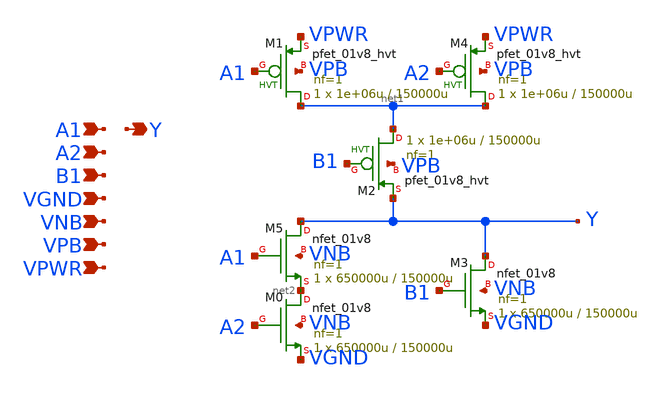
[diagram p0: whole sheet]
** sch_path: schematics/a21oi/sky130_fd_sc_hd__a21oi_1.sch
**.subckt sky130_fd_sc_hd__a21oi_1 A1 A2 B1 VGND VNB VPB VPWR Y
*.ipin A1
*.ipin A2
*.ipin B1
*.ipin VGND
*.ipin VNB
*.ipin VPB
*.ipin VPWR
*.opin Y
XM1 net1 A1 VPWR VPB sky130_fd_pr__pfet_01v8_hvt L=150000u W=1e+06u nf=1 ad='int((1 + 1)/2) * 1e+06u / 1 * 0.29'
+ as='int((1 + 2)/2) * 1e+06u / 1 * 0.29' pd='2*int((1 + 1)/2) * (1e+06u / 1 + 0.29)' ps='2*int((1 + 2)/2) * (1e+06u / 1 + 0.29)'
+ nrd='0.29 / 1e+06u ' nrs='0.29 / 1e+06u ' sa=0 sb=0 sd=0 mult=1 m=1
XM4 net1 A2 VPWR VPB sky130_fd_pr__pfet_01v8_hvt L=150000u W=1e+06u nf=1 ad='int((1 + 1)/2) * 1e+06u / 1 * 0.29'
+ as='int((1 + 2)/2) * 1e+06u / 1 * 0.29' pd='2*int((1 + 1)/2) * (1e+06u / 1 + 0.29)' ps='2*int((1 + 2)/2) * (1e+06u / 1 + 0.29)'
+ nrd='0.29 / 1e+06u ' nrs='0.29 / 1e+06u ' sa=0 sb=0 sd=0 mult=1 m=1
XM2 net1 B1 Y VPB sky130_fd_pr__pfet_01v8_hvt L=150000u W=1e+06u nf=1 ad='int((1 + 1)/2) * 1e+06u / 1 * 0.29'
+ as='int((1 + 2)/2) * 1e+06u / 1 * 0.29' pd='2*int((1 + 1)/2) * (1e+06u / 1 + 0.29)' ps='2*int((1 + 2)/2) * (1e+06u / 1 + 0.29)'
+ nrd='0.29 / 1e+06u ' nrs='0.29 / 1e+06u ' sa=0 sb=0 sd=0 mult=1 m=1
XM5 Y A1 net2 VNB sky130_fd_pr__nfet_01v8 L=150000u W=650000u nf=1 ad='int((1 + 1)/2) * 650000u / 1 * 0.29'
+ as='int((1 + 2)/2) * 650000u / 1 * 0.29' pd='2*int((1 + 1)/2) * (650000u / 1 + 0.29)' ps='2*int((1 + 2)/2) * (650000u / 1 + 0.29)'
+ nrd='0.29 / 650000u ' nrs='0.29 / 650000u ' sa=0 sb=0 sd=0 mult=1 m=1
XM0 net2 A2 VGND VNB sky130_fd_pr__nfet_01v8 L=150000u W=650000u nf=1 ad='int((1 + 1)/2) * 650000u / 1 * 0.29'
+ as='int((1 + 2)/2) * 650000u / 1 * 0.29' pd='2*int((1 + 1)/2) * (650000u / 1 + 0.29)' ps='2*int((1 + 2)/2) * (650000u / 1 + 0.29)'
+ nrd='0.29 / 650000u ' nrs='0.29 / 650000u ' sa=0 sb=0 sd=0 mult=1 m=1
XM3 Y B1 VGND VNB sky130_fd_pr__nfet_01v8 L=150000u W=650000u nf=1 ad='int((1 + 1)/2) * 650000u / 1 * 0.29'
+ as='int((1 + 2)/2) * 650000u / 1 * 0.29' pd='2*int((1 + 1)/2) * (650000u / 1 + 0.29)' ps='2*int((1 + 2)/2) * (650000u / 1 + 0.29)'
+ nrd='0.29 / 650000u ' nrs='0.29 / 650000u ' sa=0 sb=0 sd=0 mult=1 m=1
**.ends
.end
